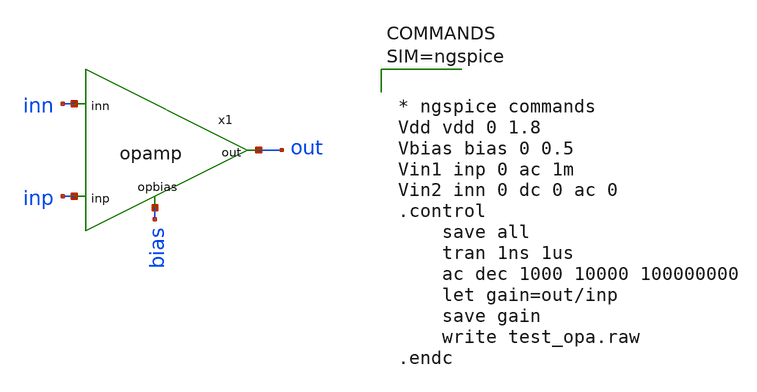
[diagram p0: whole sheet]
** sch_path: xschem/opamp/test_opa.sch
**.subckt test_opa
x1 bias inp inn out opamp
**** begin user architecture code



* ngspice commands
Vdd vdd 0 1.8
Vbias bias 0 0.5
Vin1 inp 0 ac 1m
Vin2 inn 0 dc 0 ac 0
.control
	save all
	tran 1ns 1us
	ac dec 1000 10000 100000000
	let gain=out/inp
	save gain
	write test_opa.raw
.endc




** opencircuitdesign pdks install
.lib $::SKYWATER_MODELS/sky130.lib.spice tt


**** end user architecture code
**.ends

* expanding   symbol:  opamp/opamp.sym # of pins=4
** sym_path: xschem/opamp/opamp.sym
** sch_path: xschem/opamp/opamp.sch
.subckt opamp opbias inp inn out
*.ipin inp
*.ipin inn
*.ipin opbias
*.opin out
XC1 net5 out sky130_fd_pr__cap_mim_m3_1 W=2 L=4 MF=1 m=1
XC2 out net4 sky130_fd_pr__cap_mim_m3_1 W=2 L=4 MF=1 m=1
XM26 net2 opbias VDD VDD sky130_fd_pr__pfet_01v8_lvt L=3 W=10 nf=4 ad='int((4 + 1)/2) * 10 / 4 * 0.29'
+ as='int((4 + 2)/2) * 10 / 4 * 0.29' pd='2*int((4 + 1)/2) * (10 / 4 + 0.29)' ps='2*int((4 + 2)/2) * (10 / 4 + 0.29)'
+ nrd='0.29 / 10 ' nrs='0.29 / 10 ' sa=0 sb=0 sd=0 mult=1 m=1
XM3 net1 net1 VDD VDD sky130_fd_pr__pfet_01v8_lvt L=3 W=10 nf=2 ad='int((2 + 1)/2) * 10 / 2 * 0.29' as='int((2 + 2)/2) * 10 / 2 * 0.29'
+ pd='2*int((2 + 1)/2) * (10 / 2 + 0.29)' ps='2*int((2 + 2)/2) * (10 / 2 + 0.29)' nrd='0.29 / 10 ' nrs='0.29 / 10 '
+ sa=0 sb=0 sd=0 mult=1 m=1
XM4 net5 net1 VDD VDD sky130_fd_pr__pfet_01v8_lvt L=3 W=10 nf=2 ad='int((2 + 1)/2) * 10 / 2 * 0.29' as='int((2 + 2)/2) * 10 / 2 * 0.29'
+ pd='2*int((2 + 1)/2) * (10 / 2 + 0.29)' ps='2*int((2 + 2)/2) * (10 / 2 + 0.29)' nrd='0.29 / 10 ' nrs='0.29 / 10 '
+ sa=0 sb=0 sd=0 mult=1 m=1
XM10 out net5 VDD VDD sky130_fd_pr__pfet_01v8_lvt L=3 W=100 nf=5 ad='int((5 + 1)/2) * 100 / 5 * 0.29'
+ as='int((5 + 2)/2) * 100 / 5 * 0.29' pd='2*int((5 + 1)/2) * (100 / 5 + 0.29)' ps='2*int((5 + 2)/2) * (100 / 5 + 0.29)'
+ nrd='0.29 / 100 ' nrs='0.29 / 100 ' sa=0 sb=0 sd=0 mult=1 m=1
XM14 net3 inn net2 net2 sky130_fd_pr__pfet_01v8_lvt L=3 W=15 nf=3 ad='int((3 + 1)/2) * 15 / 3 * 0.29'
+ as='int((3 + 2)/2) * 15 / 3 * 0.29' pd='2*int((3 + 1)/2) * (15 / 3 + 0.29)' ps='2*int((3 + 2)/2) * (15 / 3 + 0.29)'
+ nrd='0.29 / 15 ' nrs='0.29 / 15 ' sa=0 sb=0 sd=0 mult=1 m=1
XM15 net4 inp net2 net2 sky130_fd_pr__pfet_01v8_lvt L=3 W=15 nf=3 ad='int((3 + 1)/2) * 15 / 3 * 0.29'
+ as='int((3 + 2)/2) * 15 / 3 * 0.29' pd='2*int((3 + 1)/2) * (15 / 3 + 0.29)' ps='2*int((3 + 2)/2) * (15 / 3 + 0.29)'
+ nrd='0.29 / 15 ' nrs='0.29 / 15 ' sa=0 sb=0 sd=0 mult=1 m=1
XM17 out net4 GND GND sky130_fd_pr__nfet_01v8_lvt L=3 W=80 nf=5 ad='int((5 + 1)/2) * 80 / 5 * 0.29' as='int((5 + 2)/2) * 80 / 5 * 0.29'
+ pd='2*int((5 + 1)/2) * (80 / 5 + 0.29)' ps='2*int((5 + 2)/2) * (80 / 5 + 0.29)' nrd='0.29 / 80 ' nrs='0.29 / 80 '
+ sa=0 sb=0 sd=0 mult=1 m=1
XM19 net4 net3 GND GND sky130_fd_pr__nfet_01v8_lvt L=3 W=5 nf=1 ad='int((1 + 1)/2) * 5 / 1 * 0.29' as='int((1 + 2)/2) * 5 / 1 * 0.29'
+ pd='2*int((1 + 1)/2) * (5 / 1 + 0.29)' ps='2*int((1 + 2)/2) * (5 / 1 + 0.29)' nrd='0.29 / 5 ' nrs='0.29 / 5 '
+ sa=0 sb=0 sd=0 mult=1 m=1
XM20 net3 net3 GND GND sky130_fd_pr__nfet_01v8_lvt L=3 W=5 nf=1 ad='int((1 + 1)/2) * 5 / 1 * 0.29' as='int((1 + 2)/2) * 5 / 1 * 0.29'
+ pd='2*int((1 + 1)/2) * (5 / 1 + 0.29)' ps='2*int((1 + 2)/2) * (5 / 1 + 0.29)' nrd='0.29 / 5 ' nrs='0.29 / 5 '
+ sa=0 sb=0 sd=0 mult=1 m=1
XM2 net1 net4 GND GND sky130_fd_pr__nfet_01v8_lvt L=3 W=8 nf=1 ad='int((1 + 1)/2) * 8 / 1 * 0.29' as='int((1 + 2)/2) * 8 / 1 * 0.29'
+ pd='2*int((1 + 1)/2) * (8 / 1 + 0.29)' ps='2*int((1 + 2)/2) * (8 / 1 + 0.29)' nrd='0.29 / 8 ' nrs='0.29 / 8 '
+ sa=0 sb=0 sd=0 mult=1 m=1
XM5 net5 net3 GND GND sky130_fd_pr__nfet_01v8_lvt L=3 W=8 nf=1 ad='int((1 + 1)/2) * 8 / 1 * 0.29' as='int((1 + 2)/2) * 8 / 1 * 0.29'
+ pd='2*int((1 + 1)/2) * (8 / 1 + 0.29)' ps='2*int((1 + 2)/2) * (8 / 1 + 0.29)' nrd='0.29 / 8 ' nrs='0.29 / 8 '
+ sa=0 sb=0 sd=0 mult=1 m=1
.ends

.GLOBAL VDD
.GLOBAL GND
.end
